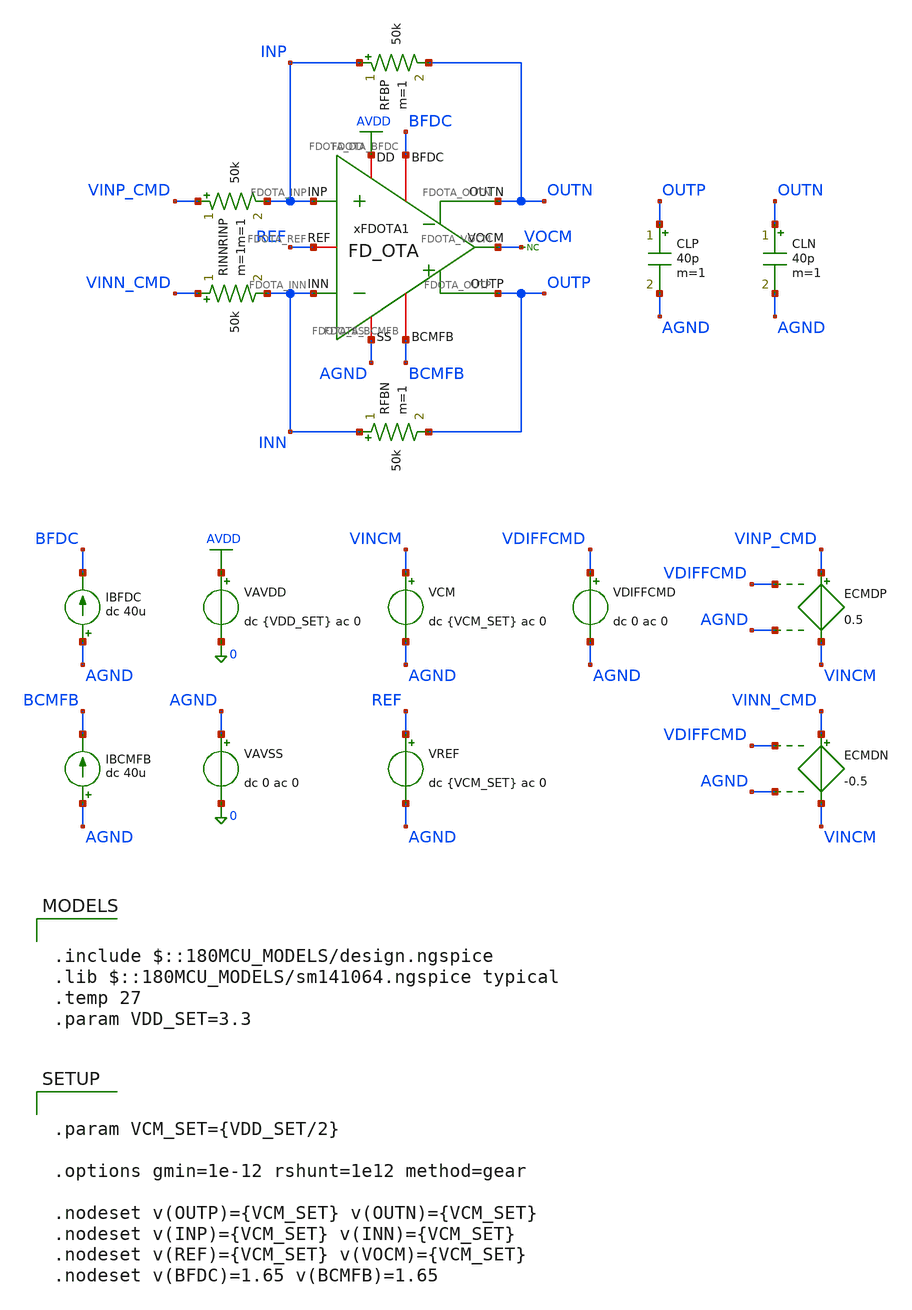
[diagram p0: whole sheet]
** sch_path: Design_Files/IC Design/Testbench/FD_OTA/FDOTA/Close_Loop/FD_OTA_TB_CL_NOM.sch
**.subckt FD_OTA_TB_CL_NOM
IBFDC AGND BFDC dc 40u
VAVDD AVDD 0 dc {VDD_SET} ac 0
.save i(vavdd)
VCM VINCM AGND dc {VCM_SET} ac 0
VDIFFCMD VDIFFCMD AGND dc 0 ac 0
VAVSS AGND 0 dc 0 ac 0
.save i(vavss)
VREF REF AGND dc {VCM_SET} ac 0
IBCMFB AGND BCMFB dc 40u
CLP OUTP AGND 40p m=1
CLN OUTN AGND 40p m=1
* noconn VOCM
ECMDP VINP_CMD VINCM VDIFFCMD AGND 0.5
ECMDN VINN_CMD VINCM VDIFFCMD AGND -0.5
RINP VINP_CMD INP 50k m=1
RINN VINN_CMD INN 50k m=1
RFBP INP OUTN 50k m=1
RFBN INN OUTP 50k m=1
xFDOTA1 AVDD AGND INP INN OUTN BFDC OUTP BCMFB REF VOCM FD_OTA
**** begin user architecture code

.include $::180MCU_MODELS/design.ngspice
.lib $::180MCU_MODELS/sm141064.ngspice typical
.temp 27
.param VDD_SET=3.3




.control
destroy all
save all
set wr_vecnames
set wr_singlescale
option numdgt=15

shell mkdir -p
+ /foss/designs/ECG_Acquisition_IC/Measurement_Results/IC_Simulation/FD_OTA/FDOTA/NOM.Result_txt

shell rm -f
+ /foss/designs/ECG_Acquisition_IC/Measurement_Results/IC_Simulation/FD_OTA/FDOTA/NOM.Result_txt/NOM.cl_diff_dc.txt
shell rm -f
+ /foss/designs/ECG_Acquisition_IC/Measurement_Results/IC_Simulation/FD_OTA/FDOTA/NOM.Result_txt/NOM.cl_icmr.txt
shell rm -f
+ /foss/designs/ECG_Acquisition_IC/Measurement_Results/IC_Simulation/FD_OTA/FDOTA/NOM.Result_txt/NOM.cl_diff_tran.txt
shell rm -f
+ /foss/designs/ECG_Acquisition_IC/Measurement_Results/IC_Simulation/FD_OTA/FDOTA/NOM.Result_txt/NOM.cl_cm_tran.txt

* DC
op
let avdd_run = v(AVDD)-v(AGND)
let vcm_run = avdd_run/2
let vdiff_low = -avdd_run
let vdiff_high = avdd_run

alter @VCM[DC] = $&vcm_run
alter @VREF[DC] = $&vcm_run
alter @VDIFFCMD[DC] = 0

dc VDIFFCMD $&vdiff_low $&vdiff_high 0.001

let cl_vin_diff = v(INP)-v(INN)
let cl_voutcm = 0.5*(v(OUTP)+v(OUTN))
let cl_voutdiff = v(OUTP)-v(OUTN)
let cl_idd = -vavdd#branch

setscale v(VDIFFCMD)

wrdata
+ /foss/designs/ECG_Acquisition_IC/Measurement_Results/IC_Simulation/FD_OTA/FDOTA/NOM.Result_txt/NOM.cl_diff_dc.txt cl_vin_diff v(OUTP) v(OUTN) cl_voutcm cl_voutdiff v(VOCM) cl_idd

* ICMR
reset
save all
set wr_vecnames
set wr_singlescale
option numdgt=15

op
let avdd_run = v(AVDD)-v(AGND)
let vref_run = avdd_run/2
let vcm_low_sweep = 0
let vcm_high_sweep = avdd_run

alter @VREF[DC] = $&vref_run
alter @VDIFFCMD[DC] = 0

dc VCM $&vcm_low_sweep $&vcm_high_sweep 0.001 VDIFFCMD -20m 20m 2m

let icmr_vin_cm = 0.5*(v(INP)+v(INN))
let icmr_vin_diff = v(INP)-v(INN)
let icmr_voutcm = 0.5*(v(OUTP)+v(OUTN))
let icmr_voutdiff = v(OUTP)-v(OUTN)
let icmr_idd = -vavdd#branch

setscale icmr_vin_cm

wrdata
+ /foss/designs/ECG_Acquisition_IC/Measurement_Results/IC_Simulation/FD_OTA/FDOTA/NOM.Result_txt/NOM.cl_icmr.txt v(VINCM) v(REF) v(BCMFB) v(VDIFFCMD) icmr_vin_diff v(OUTP) v(OUTN) icmr_voutcm icmr_voutdiff
+ v(VOCM) icmr_idd

* Tran
reset
save all
set wr_vecnames
set wr_singlescale
option numdgt=15

op
let avdd_run = v(AVDD)-v(AGND)
let vcm_run = avdd_run/2

alter @VCM[DC] = $&vcm_run
alter @VREF[DC] = $&vcm_run
alter @VDIFFCMD[PWL] = [ 0 0 1u 0 1.001u 1.0 11u 1.0 11.001u 0 21u 0 21.001u -1.0 31u -1.0 31.001u 0
+ 40u 0 ]

tran 0.5n 40u

let tr_vin_diff = v(INP)-v(INN)
let tr_voutcm = 0.5*(v(OUTP)+v(OUTN))
let tr_voutdiff = v(OUTP)-v(OUTN)
let tr_idd = -vavdd#branch

setscale time

wrdata
+ /foss/designs/ECG_Acquisition_IC/Measurement_Results/IC_Simulation/FD_OTA/FDOTA/NOM.Result_txt/NOM.cl_diff_tran.txt v(VDIFFCMD) tr_vin_diff v(OUTP) v(OUTN) tr_voutcm tr_voutdiff v(VOCM) tr_idd

* CM tran
reset
save all
set wr_vecnames
set wr_singlescale
option numdgt=15

op
let avdd_run = v(AVDD)-v(AGND)
let vcm_run = avdd_run/2
let vref_low_step = vcm_run - 0.80
let vref_high_step = vcm_run + 0.80

alter @VDIFFCMD[PWL] = [ 0 0 40u 0 ]
alter @VREF[PWL] = [ 0 $&vref_low_step 1u $&vref_low_step 1.001u $&vcm_run 11u $&vcm_run 11.001u
+ $&vref_high_step 21u $&vref_high_step 21.001u $&vcm_run 40u $&vcm_run ]

tran 0.5n 40u

let cm_voutcm = 0.5*(v(OUTP)+v(OUTN))
let cm_voutdiff = v(OUTP)-v(OUTN)
let cm_idd = -vavdd#branch

setscale time

wrdata
+ /foss/designs/ECG_Acquisition_IC/Measurement_Results/IC_Simulation/FD_OTA/FDOTA/NOM.Result_txt/NOM.cl_cm_tran.txt v(REF) v(VOCM) v(OUTP) v(OUTN) cm_voutcm cm_voutdiff cm_idd

quit
.endc




.param VCM_SET={VDD_SET/2}

.options gmin=1e-12 rshunt=1e12 method=gear

.nodeset v(OUTP)={VCM_SET} v(OUTN)={VCM_SET}
.nodeset v(INP)={VCM_SET} v(INN)={VCM_SET}
.nodeset v(REF)={VCM_SET} v(VOCM)={VCM_SET}
.nodeset v(BFDC)=1.65 v(BCMFB)=1.65


**** end user architecture code
**.ends

* expanding   symbol:  ECG_Acquisition_IC/Design_Files/IC Design/Schematic/FD_OTA/FDOTA/FD_OTA.sym #
*+ of pins=10
** sym_path: Design_Files/IC Design/Schematic/FD_OTA/FDOTA/FD_OTA.sym
** sch_path: Design_Files/IC Design/Schematic/FD_OTA/FDOTA/FD_OTA.sch
.subckt FD_OTA FDOTA_DD FDOTA_SS FDOTA_INP FDOTA_INN FDOTA_OUTN FDOTA_BFDC FDOTA_OUTP FDOTA_BCMFB
+ FDOTA_REF FDOTA_VOCM
*.iopin FDOTA_DD
*.iopin FDOTA_SS
*.ipin FDOTA_INP
*.ipin FDOTA_INN
*.opin FDOTA_OUTP
*.iopin FDOTA_BFDC
*.opin FDOTA_OUTN
*.iopin FDOTA_BCMFB
*.iopin FDOTA_REF
*.iopin FDOTA_VOCM
R1 FDOTA_OUTP FDOTA_VOCM 100k m=1
R2 FDOTA_VOCM FDOTA_OUTN 100k m=1
C1 FDOTA_OUTP FDOTA_VOCM 50f m=1
C2 FDOTA_VOCM FDOTA_OUTN 50f m=1
xFDC1 FDOTA_DD FDOTA_SS FDOTA_INP FDOTA_INN FDOTA_OUTN FDOTA_BFDC FDOTA_OUTP FDOTA_VCMFB FDC
xCMFB1 FDOTA_DD FDOTA_SS FDOTA_VOCM FDOTA_REF FDOTA_VCMFB FDOTA_BCMFB CMFB
.ends


* expanding   symbol:  ECG_Acquisition_IC/Design_Files/IC Design/Schematic/FD_OTA/FDC/FDC.sym # of
*+ pins=8
** sym_path: Design_Files/IC Design/Schematic/FD_OTA/FDC/FDC.sym
** sch_path: Design_Files/IC Design/Schematic/FD_OTA/FDC/FDC.sch
.subckt FDC FDC_DD FDC_SS FDC_INP FDC_INN FDC_OUTN FDC_B FDC_OUTP FDC_CMFB
*.iopin FDC_DD
*.iopin FDC_SS
*.ipin FDC_INP
*.ipin FDC_INN
*.opin FDC_OUTP
*.iopin FDC_B
*.opin FDC_OUTN
*.iopin FDC_CMFB
XM3 net4 FDC_CMFB FDC_DD FDC_DD pfet_03v3 L=2u W=1u nf=1 ad='int((nf+1)/2) * W/nf * 0.18u' as='int((nf+2)/2) * W/nf * 0.18u'
+ pd='2*int((nf+1)/2) * (W/nf + 0.18u)' ps='2*int((nf+2)/2) * (W/nf + 0.18u)' nrd='0.18u / W' nrs='0.18u / W'
+ sa=0 sb=0 sd=0 m=200
XM8 FDC_OUTP FDC_B FDC_SS FDC_SS nfet_03v3 L=0.5u W=1u nf=1 ad='int((nf+1)/2) * W/nf * 0.18u' as='int((nf+2)/2) * W/nf * 0.18u'
+ pd='2*int((nf+1)/2) * (W/nf + 0.18u)' ps='2*int((nf+2)/2) * (W/nf + 0.18u)' nrd='0.18u / W' nrs='0.18u / W'
+ sa=0 sb=0 sd=0 m=100
Rz net1 net2 3.5k m=1
XM5 net3 FDC_B FDC_SS FDC_SS nfet_03v3 L=2u W=1u nf=1 ad='int((nf+1)/2) * W/nf * 0.18u' as='int((nf+2)/2) * W/nf * 0.18u'
+ pd='2*int((nf+1)/2) * (W/nf + 0.18u)' ps='2*int((nf+2)/2) * (W/nf + 0.18u)' nrd='0.18u / W' nrs='0.18u / W'
+ sa=0 sb=0 sd=0 m=10
XM6 FDC_OUTP net1 FDC_DD FDC_DD pfet_03v3 L=0.5u W=1u nf=1 ad='int((nf+1)/2) * W/nf * 0.18u' as='int((nf+2)/2) * W/nf * 0.18u'
+ pd='2*int((nf+1)/2) * (W/nf + 0.18u)' ps='2*int((nf+2)/2) * (W/nf + 0.18u)' nrd='0.18u / W' nrs='0.18u / W'
+ sa=0 sb=0 sd=0 m=200
XM10 FDC_B FDC_B FDC_SS FDC_SS nfet_03v3 L=2u W=1u nf=1 ad='int((nf+1)/2) * W/nf * 0.18u' as='int((nf+2)/2) * W/nf * 0.18u'
+ pd='2*int((nf+1)/2) * (W/nf + 0.18u)' ps='2*int((nf+2)/2) * (W/nf + 0.18u)' nrd='0.18u / W' nrs='0.18u / W'
+ sa=0 sb=0 sd=0 m=20
Cc net2 FDC_OUTP 2.5p m=1
XM9 FDC_OUTN FDC_B FDC_SS FDC_SS nfet_03v3 L=0.5u W=1u nf=1 ad='int((nf+1)/2) * W/nf * 0.18u' as='int((nf+2)/2) * W/nf * 0.18u'
+ pd='2*int((nf+1)/2) * (W/nf + 0.18u)' ps='2*int((nf+2)/2) * (W/nf + 0.18u)' nrd='0.18u / W' nrs='0.18u / W'
+ sa=0 sb=0 sd=0 m=100
Rz1 net4 net5 3.5k m=1
XM7 FDC_OUTN net4 FDC_DD FDC_DD pfet_03v3 L=0.5u W=1u nf=1 ad='int((nf+1)/2) * W/nf * 0.18u' as='int((nf+2)/2) * W/nf * 0.18u'
+ pd='2*int((nf+1)/2) * (W/nf + 0.18u)' ps='2*int((nf+2)/2) * (W/nf + 0.18u)' nrd='0.18u / W' nrs='0.18u / W'
+ sa=0 sb=0 sd=0 m=200
Cc1 net5 FDC_OUTN 2.5p m=1
XM4 net1 FDC_CMFB FDC_DD FDC_DD pfet_03v3 L=2u W=1u nf=1 ad='int((nf+1)/2) * W/nf * 0.18u' as='int((nf+2)/2) * W/nf * 0.18u'
+ pd='2*int((nf+1)/2) * (W/nf + 0.18u)' ps='2*int((nf+2)/2) * (W/nf + 0.18u)' nrd='0.18u / W' nrs='0.18u / W'
+ sa=0 sb=0 sd=0 m=200
XM1 net4 FDC_INN net3 FDC_SS nfet_03v3 L=2u W=1u nf=1 ad='int((nf+1)/2) * W/nf * 0.18u' as='int((nf+2)/2) * W/nf * 0.18u'
+ pd='2*int((nf+1)/2) * (W/nf + 0.18u)' ps='2*int((nf+2)/2) * (W/nf + 0.18u)' nrd='0.18u / W' nrs='0.18u / W'
+ sa=0 sb=0 sd=0 m=200
XM2 net1 FDC_INP net3 FDC_SS nfet_03v3 L=2u W=1u nf=1 ad='int((nf+1)/2) * W/nf * 0.18u' as='int((nf+2)/2) * W/nf * 0.18u'
+ pd='2*int((nf+1)/2) * (W/nf + 0.18u)' ps='2*int((nf+2)/2) * (W/nf + 0.18u)' nrd='0.18u / W' nrs='0.18u / W'
+ sa=0 sb=0 sd=0 m=200
.ends


* expanding   symbol:  ECG_Acquisition_IC/Design_Files/IC Design/Schematic/FD_OTA/CMFB/CMFB.sym # of
*+ pins=6
** sym_path: Design_Files/IC Design/Schematic/FD_OTA/CMFB/CMFB.sym
** sch_path: Design_Files/IC Design/Schematic/FD_OTA/CMFB/CMFB.sch
.subckt CMFB CMFB_DD CMFB_SS CMFB_IN CMFB_REF CMFB_OUT CMFB_B
*.iopin CMFB_DD
*.iopin CMFB_SS
*.ipin CMFB_IN
*.ipin CMFB_REF
*.opin CMFB_OUT
*.iopin CMFB_B
XM4 CMFB_OUT CMFB_OUT CMFB_DD CMFB_DD pfet_03v3 L=0.5u W=1u nf=1 ad='int((nf+1)/2) * W/nf * 0.18u' as='int((nf+2)/2) * W/nf * 0.18u'
+ pd='2*int((nf+1)/2) * (W/nf + 0.18u)' ps='2*int((nf+2)/2) * (W/nf + 0.18u)' nrd='0.18u / W' nrs='0.18u / W'
+ sa=0 sb=0 sd=0 m=77
XM3 net2 net2 CMFB_DD CMFB_DD pfet_03v3 L=0.5u W=1u nf=1 ad='int((nf+1)/2) * W/nf * 0.18u' as='int((nf+2)/2) * W/nf * 0.18u'
+ pd='2*int((nf+1)/2) * (W/nf + 0.18u)' ps='2*int((nf+2)/2) * (W/nf + 0.18u)' nrd='0.18u / W' nrs='0.18u / W'
+ sa=0 sb=0 sd=0 m=77
XM1 net2 CMFB_REF net1 CMFB_SS nfet_03v3 L=0.5u W=1u nf=1 ad='int((nf+1)/2) * W/nf * 0.18u' as='int((nf+2)/2) * W/nf * 0.18u'
+ pd='2*int((nf+1)/2) * (W/nf + 0.18u)' ps='2*int((nf+2)/2) * (W/nf + 0.18u)' nrd='0.18u / W' nrs='0.18u / W'
+ sa=0 sb=0 sd=0 m=5
XM2 CMFB_OUT CMFB_IN net1 CMFB_SS nfet_03v3 L=0.5u W=1u nf=1 ad='int((nf+1)/2) * W/nf * 0.18u' as='int((nf+2)/2) * W/nf * 0.18u'
+ pd='2*int((nf+1)/2) * (W/nf + 0.18u)' ps='2*int((nf+2)/2) * (W/nf + 0.18u)' nrd='0.18u / W' nrs='0.18u / W'
+ sa=0 sb=0 sd=0 m=5
XM5 net1 CMFB_B CMFB_SS CMFB_SS nfet_03v3 L=2u W=1u nf=1 ad='int((nf+1)/2) * W/nf * 0.18u' as='int((nf+2)/2) * W/nf * 0.18u'
+ pd='2*int((nf+1)/2) * (W/nf + 0.18u)' ps='2*int((nf+2)/2) * (W/nf + 0.18u)' nrd='0.18u / W' nrs='0.18u / W'
+ sa=0 sb=0 sd=0 m=20
XM10 CMFB_B CMFB_B CMFB_SS CMFB_SS nfet_03v3 L=2u W=1u nf=1 ad='int((nf+1)/2) * W/nf * 0.18u' as='int((nf+2)/2) * W/nf * 0.18u'
+ pd='2*int((nf+1)/2) * (W/nf + 0.18u)' ps='2*int((nf+2)/2) * (W/nf + 0.18u)' nrd='0.18u / W' nrs='0.18u / W'
+ sa=0 sb=0 sd=0 m=20
.ends

.GLOBAL AVDD
.end
